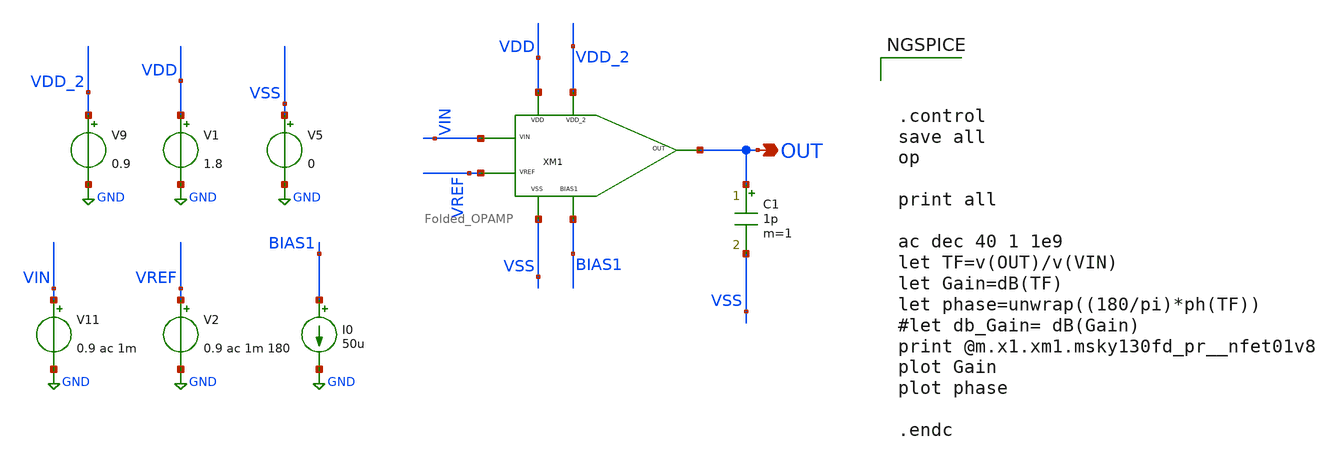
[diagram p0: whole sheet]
** sch_path: xschem/DC_DC_Converter_xschem/OTHERS/DC_DC_Converter_JV10/Folded_OPAMP_v2/tb_Folded_OPAMP.sch
**.subckt tb_Folded_OPAMP OUT
*.opin OUT
I0 BIAS1 GND 50u
V9 VDD_2 GND 0.9
V1 VDD GND 1.8
V5 VSS GND 0
V11 VIN GND 0.9 ac 1m
V2 VREF GND 0.9 ac 1m 180
C1 OUT VSS 1p m=1
XM1 VDD VSS VDD_2 BIAS1 OUT VIN VREF Folded_OPAMP
**** begin user architecture code

** opencircuitdesign pdks install
.lib $::SKYWATER_MODELS/sky130.lib.spice tt





.control
save all
op

print all

ac dec 40 1 1e9
let TF=v(OUT)/v(VIN)
let Gain=dB(TF)
let phase=unwrap((180/pi)*ph(TF))
#let db_Gain= dB(Gain)
print @m.x1.xm1.msky130fd_pr__nfet01v8
plot Gain
plot phase

.endc


**** end user architecture code
**.ends

* expanding   symbol:  DC_DC_Converter/Folded_OPAMP_v2/Folded_OPAMP.sym # of pins=7
** sym_path: xschem/DC_DC_Converter_xschem/OTHERS/DC_DC_Converter_JV10/Folded_OPAMP_v2/Folded_OPAMP.sym
** sch_path: xschem/DC_DC_Converter_xschem/OTHERS/DC_DC_Converter_JV10/Folded_OPAMP_v2/Folded_OPAMP.sch
.subckt Folded_OPAMP VDD VSS VDD_2 BIAS1 OUT VIN VREF
*.iopin VSS
*.iopin VDD
*.iopin VDD_2
*.opin OUT
*.ipin VIN
*.ipin VREF
*.iopin BIAS1
XM13 VDD_2 VDD_2 BIAS2 VSS sky130_fd_pr__nfet_01v8 L=0.9 W=5.14 nf=1 ad='int((nf+1)/2) * W/nf * 0.29'
+ as='int((nf+2)/2) * W/nf * 0.29' pd='2*int((nf+1)/2) * (W/nf + 0.29)' ps='2*int((nf+2)/2) * (W/nf + 0.29)'
+ nrd='0.29 / W' nrs='0.29 / W' sa=0 sb=0 sd=0 mult=1 m=1
XM14 BIAS3 BIAS3 net4 VSS sky130_fd_pr__nfet_01v8 L=0.9 W=7.714 nf=10 ad='int((nf+1)/2) * W/nf * 0.29'
+ as='int((nf+2)/2) * W/nf * 0.29' pd='2*int((nf+1)/2) * (W/nf + 0.29)' ps='2*int((nf+2)/2) * (W/nf + 0.29)'
+ nrd='0.29 / W' nrs='0.29 / W' sa=0 sb=0 sd=0 mult=1 m=1
XM15 BIAS2 BIAS2 VSS VSS sky130_fd_pr__nfet_01v8 L=0.9 W=5.14 nf=1 ad='int((nf+1)/2) * W/nf * 0.29' as='int((nf+2)/2) * W/nf * 0.29'
+ pd='2*int((nf+1)/2) * (W/nf + 0.29)' ps='2*int((nf+2)/2) * (W/nf + 0.29)' nrd='0.29 / W' nrs='0.29 / W'
+ sa=0 sb=0 sd=0 mult=1 m=1
XM17 VOUTP VIN net5 VSS sky130_fd_pr__nfet_01v8 L=0.9 W=2 nf=5 ad='int((nf+1)/2) * W/nf * 0.29' as='int((nf+2)/2) * W/nf * 0.29'
+ pd='2*int((nf+1)/2) * (W/nf + 0.29)' ps='2*int((nf+2)/2) * (W/nf + 0.29)' nrd='0.29 / W' nrs='0.29 / W'
+ sa=0 sb=0 sd=0 mult=8 m=8
XM9 net5 net4 VSS VSS sky130_fd_pr__nfet_01v8 L=0.9 W=2 nf=2 ad='int((nf+1)/2) * W/nf * 0.29' as='int((nf+2)/2) * W/nf * 0.29'
+ pd='2*int((nf+1)/2) * (W/nf + 0.29)' ps='2*int((nf+2)/2) * (W/nf + 0.29)' nrd='0.29 / W' nrs='0.29 / W'
+ sa=0 sb=0 sd=0 mult=2 m=2
XM1 BIAS1 BIAS1 VDD VDD sky130_fd_pr__pfet_01v8 L=0.9 W=7.714 nf=1 ad='int((nf+1)/2) * W/nf * 0.29' as='int((nf+2)/2) * W/nf * 0.29'
+ pd='2*int((nf+1)/2) * (W/nf + 0.29)' ps='2*int((nf+2)/2) * (W/nf + 0.29)' nrd='0.29 / W' nrs='0.29 / W'
+ sa=0 sb=0 sd=0 mult=1 m=1
XM2 BIAS3 BIAS1 VDD VDD sky130_fd_pr__pfet_01v8 L=0.9 W=7.714 nf=1 ad='int((nf+1)/2) * W/nf * 0.29' as='int((nf+2)/2) * W/nf * 0.29'
+ pd='2*int((nf+1)/2) * (W/nf + 0.29)' ps='2*int((nf+2)/2) * (W/nf + 0.29)' nrd='0.29 / W' nrs='0.29 / W'
+ sa=0 sb=0 sd=0 mult=1 m=1
XM18 VOUTN VREF net5 VSS sky130_fd_pr__nfet_01v8 L=0.9 W=2 nf=5 ad='int((nf+1)/2) * W/nf * 0.29' as='int((nf+2)/2) * W/nf * 0.29'
+ pd='2*int((nf+1)/2) * (W/nf + 0.29)' ps='2*int((nf+2)/2) * (W/nf + 0.29)' nrd='0.29 / W' nrs='0.29 / W'
+ sa=0 sb=0 sd=0 mult=8 m=8
XM8 net5 net4 VSS VSS sky130_fd_pr__nfet_01v8 L=0.9 W=8 nf=2 ad='int((nf+1)/2) * W/nf * 0.29' as='int((nf+2)/2) * W/nf * 0.29'
+ pd='2*int((nf+1)/2) * (W/nf + 0.29)' ps='2*int((nf+2)/2) * (W/nf + 0.29)' nrd='0.29 / W' nrs='0.29 / W'
+ sa=0 sb=0 sd=0 mult=2 m=2
XM4 VOUTP BIAS1 VDD VDD sky130_fd_pr__pfet_01v8 L=1 W=2 nf=10 ad='int((nf+1)/2) * W/nf * 0.29' as='int((nf+2)/2) * W/nf * 0.29'
+ pd='2*int((nf+1)/2) * (W/nf + 0.29)' ps='2*int((nf+2)/2) * (W/nf + 0.29)' nrd='0.29 / W' nrs='0.29 / W'
+ sa=0 sb=0 sd=0 mult=5 m=5
XM3 VOUTN BIAS1 VDD VDD sky130_fd_pr__pfet_01v8 L=0.9 W=2 nf=5 ad='int((nf+1)/2) * W/nf * 0.29' as='int((nf+2)/2) * W/nf * 0.29'
+ pd='2*int((nf+1)/2) * (W/nf + 0.29)' ps='2*int((nf+2)/2) * (W/nf + 0.29)' nrd='0.29 / W' nrs='0.29 / W'
+ sa=0 sb=0 sd=0 mult=10 m=10
XM6 net3 BIAS2 VOUTP VDD sky130_fd_pr__pfet_01v8 L=0.9 W=2 nf=5 ad='int((nf+1)/2) * W/nf * 0.29' as='int((nf+2)/2) * W/nf * 0.29'
+ pd='2*int((nf+1)/2) * (W/nf + 0.29)' ps='2*int((nf+2)/2) * (W/nf + 0.29)' nrd='0.29 / W' nrs='0.29 / W'
+ sa=0 sb=0 sd=0 mult=10 m=10
XM7 OUT BIAS2 VOUTN VDD sky130_fd_pr__pfet_01v8 L=0.9 W=2 nf=5 ad='int((nf+1)/2) * W/nf * 0.29' as='int((nf+2)/2) * W/nf * 0.29'
+ pd='2*int((nf+1)/2) * (W/nf + 0.29)' ps='2*int((nf+2)/2) * (W/nf + 0.29)' nrd='0.29 / W' nrs='0.29 / W'
+ sa=0 sb=0 sd=0 mult=10 m=10
XM5 OUT BIAS3 net1 VSS sky130_fd_pr__nfet_01v8 L=0.9 W=2 nf=5 ad='int((nf+1)/2) * W/nf * 0.29' as='int((nf+2)/2) * W/nf * 0.29'
+ pd='2*int((nf+1)/2) * (W/nf + 0.29)' ps='2*int((nf+2)/2) * (W/nf + 0.29)' nrd='0.29 / W' nrs='0.29 / W'
+ sa=0 sb=0 sd=0 mult=2 m=2
XM10 net1 net3 VSS VSS sky130_fd_pr__nfet_01v8 L=0.9 W=2 nf=5 ad='int((nf+1)/2) * W/nf * 0.29' as='int((nf+2)/2) * W/nf * 0.29'
+ pd='2*int((nf+1)/2) * (W/nf + 0.29)' ps='2*int((nf+2)/2) * (W/nf + 0.29)' nrd='0.29 / W' nrs='0.29 / W'
+ sa=0 sb=0 sd=0 mult=2 m=2
XM11 net2 net3 VSS VSS sky130_fd_pr__nfet_01v8 L=0.9 W=2 nf=5 ad='int((nf+1)/2) * W/nf * 0.29' as='int((nf+2)/2) * W/nf * 0.29'
+ pd='2*int((nf+1)/2) * (W/nf + 0.29)' ps='2*int((nf+2)/2) * (W/nf + 0.29)' nrd='0.29 / W' nrs='0.29 / W'
+ sa=0 sb=0 sd=0 mult=2 m=2
XM12 net3 BIAS3 net2 VSS sky130_fd_pr__nfet_01v8 L=0.9 W=2 nf=5 ad='int((nf+1)/2) * W/nf * 0.29' as='int((nf+2)/2) * W/nf * 0.29'
+ pd='2*int((nf+1)/2) * (W/nf + 0.29)' ps='2*int((nf+2)/2) * (W/nf + 0.29)' nrd='0.29 / W' nrs='0.29 / W'
+ sa=0 sb=0 sd=0 mult=2 m=2
XM16 net4 net4 VSS VSS sky130_fd_pr__nfet_01v8 L=0.9 W=2 nf=2 ad='int((nf+1)/2) * W/nf * 0.29' as='int((nf+2)/2) * W/nf * 0.29'
+ pd='2*int((nf+1)/2) * (W/nf + 0.29)' ps='2*int((nf+2)/2) * (W/nf + 0.29)' nrd='0.29 / W' nrs='0.29 / W'
+ sa=0 sb=0 sd=0 mult=2 m=2
.ends

.GLOBAL GND
.end
